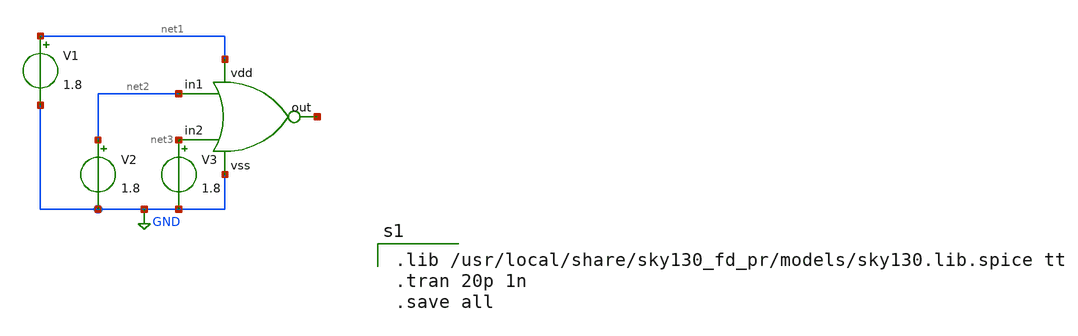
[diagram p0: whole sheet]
** sch_path: projects/carry_lookahead_adder/xschem/ports/test/true_table/nor.sch
**.subckt nor
V1 net1 GND 1.8
x1 net2 net3 net4 net1 GND nor
V2 net2 GND 1.8
V3 net3 GND 1.8
**** begin user architecture code

.lib /usr/local/share/sky130_fd_pr/models/sky130.lib.spice tt
.tran 20p 1n
.save all

**** end user architecture code
**.ends

* expanding   symbol:  nor.sym # of pins=5
** sym_path: projects/carry_lookahead_adder/xschem/ports/nor.sym
** sch_path: projects/carry_lookahead_adder/xschem/ports/nor.sch
.subckt nor in1 in2 out vdd vss
*.ipin in1
*.ipin in2
*.opin out
*.ipin vdd
*.ipin vss
XM3 out in1 vss vss sky130_fd_pr__nfet_01v8 L=0.15 W=1 nf=1 ad='int((nf+1)/2) * W/nf * 0.29' as='int((nf+2)/2) * W/nf * 0.29'
+ pd='2*int((nf+1)/2) * (W/nf + 0.29)' ps='2*int((nf+2)/2) * (W/nf + 0.29)' nrd='0.29 / W' nrs='0.29 / W'
+ sa=0 sb=0 sd=0 mult=1 m=1
XM4 out in2 vss vss sky130_fd_pr__nfet_01v8 L=0.15 W=1 nf=1 ad='int((nf+1)/2) * W/nf * 0.29' as='int((nf+2)/2) * W/nf * 0.29'
+ pd='2*int((nf+1)/2) * (W/nf + 0.29)' ps='2*int((nf+2)/2) * (W/nf + 0.29)' nrd='0.29 / W' nrs='0.29 / W'
+ sa=0 sb=0 sd=0 mult=1 m=1
XM1 net1 in1 vdd net3 sky130_fd_pr__pfet_01v8 L=0.15 W=4.15 nf=1 ad='int((nf+1)/2) * W/nf * 0.29' as='int((nf+2)/2) * W/nf * 0.29'
+ pd='2*int((nf+1)/2) * (W/nf + 0.29)' ps='2*int((nf+2)/2) * (W/nf + 0.29)' nrd='0.29 / W' nrs='0.29 / W'
+ sa=0 sb=0 sd=0 mult=1 m=1
XM2 out in2 net1 net2 sky130_fd_pr__pfet_01v8 L=0.15 W=4.15 nf=1 ad='int((nf+1)/2) * W/nf * 0.29' as='int((nf+2)/2) * W/nf * 0.29'
+ pd='2*int((nf+1)/2) * (W/nf + 0.29)' ps='2*int((nf+2)/2) * (W/nf + 0.29)' nrd='0.29 / W' nrs='0.29 / W'
+ sa=0 sb=0 sd=0 mult=1 m=1
.ends

.GLOBAL GND
.end
